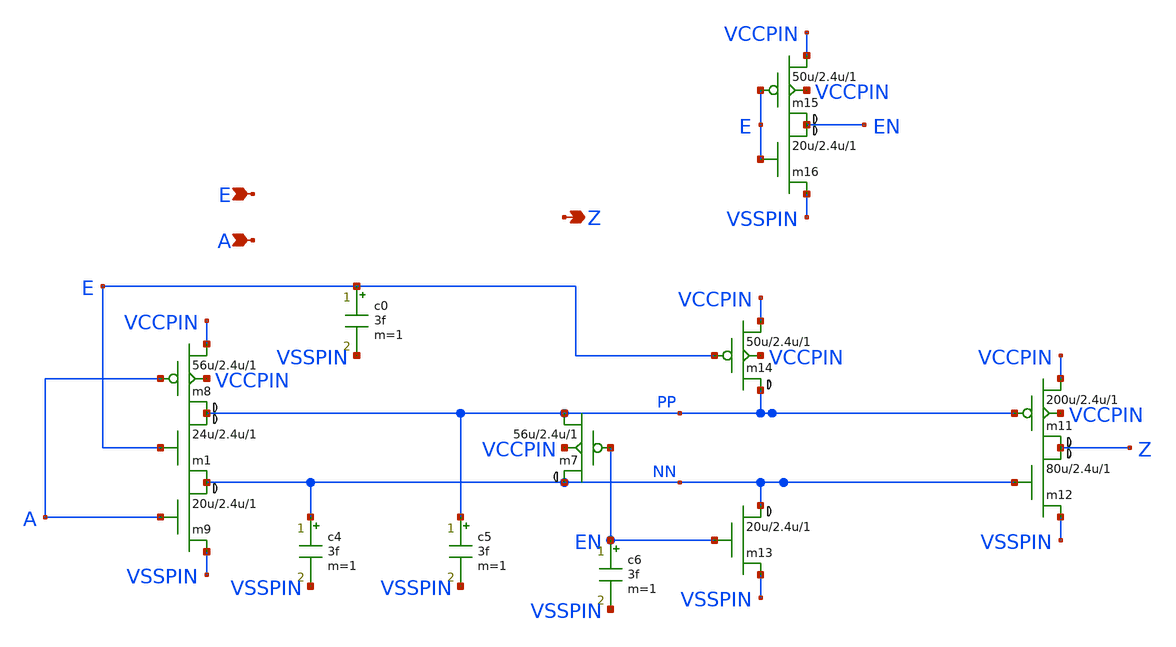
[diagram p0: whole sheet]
** sch_path: xschem_libs_newsym/rom8k/bts/schematic/bts.sch
* Copyright (C) 1998-2024 Stefan Frederik Schippers
* This program is free software; you can redistribute it and/or modify
* it under the terms of the GNU General Public License as published by
* the Free Software Foundation; either version 2 of the License, or
* (at your option) any later version.
* This program is distributed in the hope that it will be useful,
* but WITHOUT ANY WARRANTY; without even the implied warranty of
* MERCHANTABILITY or FITNESS FOR A PARTICULAR PURPOSE.  See the
* GNU General Public License for more details.
* You should have received a copy of the GNU General Public License
* along with this program; if not, write to the Free Software
**.subckt bts A E Z
*.ipin A
*.ipin E
*.opin Z
m7 NN EN PP VCCPIN cmosp w=56u l=2.4u ad={56u *2.2u} as={56u *2.2u} pd={56u *2+4.4u} ps={56u *2+4.4u}
+ m=1
m8 PP A VCCPIN VCCPIN cmosp w=56u l=2.4u ad={56u *2.2u} as={56u *2.2u} pd={56u *2+4.4u} ps={56u *2+4.4u}
+ m=1
m9 NN A VSSPIN 0 cmosn w=20u l=2.4u ad={20u *4.4u} as={20u *4.4u} pd={20u *2 + 8.8u} ps={20u *2 + 8.8u}
+ m=1
m1 PP E NN 0 cmosn w=24u l=2.4u ad={24u *4.4u} as={24u *4.4u} pd={24u *2 + 8.8u} ps={24u *2 + 8.8u} m=1
m11 Z PP VCCPIN VCCPIN cmosp w=200u l=2.4u ad={200u *2.2u} as={200u *2.2u} pd={200u *2+4.4u} ps={200u *2+4.4u}
+ m=1
m12 Z NN VSSPIN 0 cmosn w=80u l=2.4u ad={80u *4.4u} as={80u *4.4u} pd={80u *2 + 8.8u} ps={80u *2 + 8.8u}
+ m=1
m13 NN EN VSSPIN 0 cmosn w=20u l=2.4u ad={20u *4.4u} as={20u *4.4u} pd={20u *2 + 8.8u} ps={20u *2 + 8.8u}
+ m=1
m14 PP E VCCPIN VCCPIN cmosp w=50u l=2.4u ad={50u *2.2u} as={50u *2.2u} pd={50u *2+4.4u} ps={50u *2+4.4u}
+ m=1
m15 EN E VCCPIN VCCPIN cmosp w=50u l=2.4u ad={50u *2.2u} as={50u *2.2u} pd={50u *2+4.4u} ps={50u *2+4.4u}
+ m=1
m16 EN E VSSPIN 0 cmosn w=20u l=2.4u ad={20u *4.4u} as={20u *4.4u} pd={20u *2 + 8.8u} ps={20u *2 + 8.8u}
+ m=1
c0 E VSSPIN 3f m=1
c4 NN VSSPIN 3f m=1
c5 PP VSSPIN 3f m=1
c6 EN VSSPIN 3f m=1
**.ends
.end
